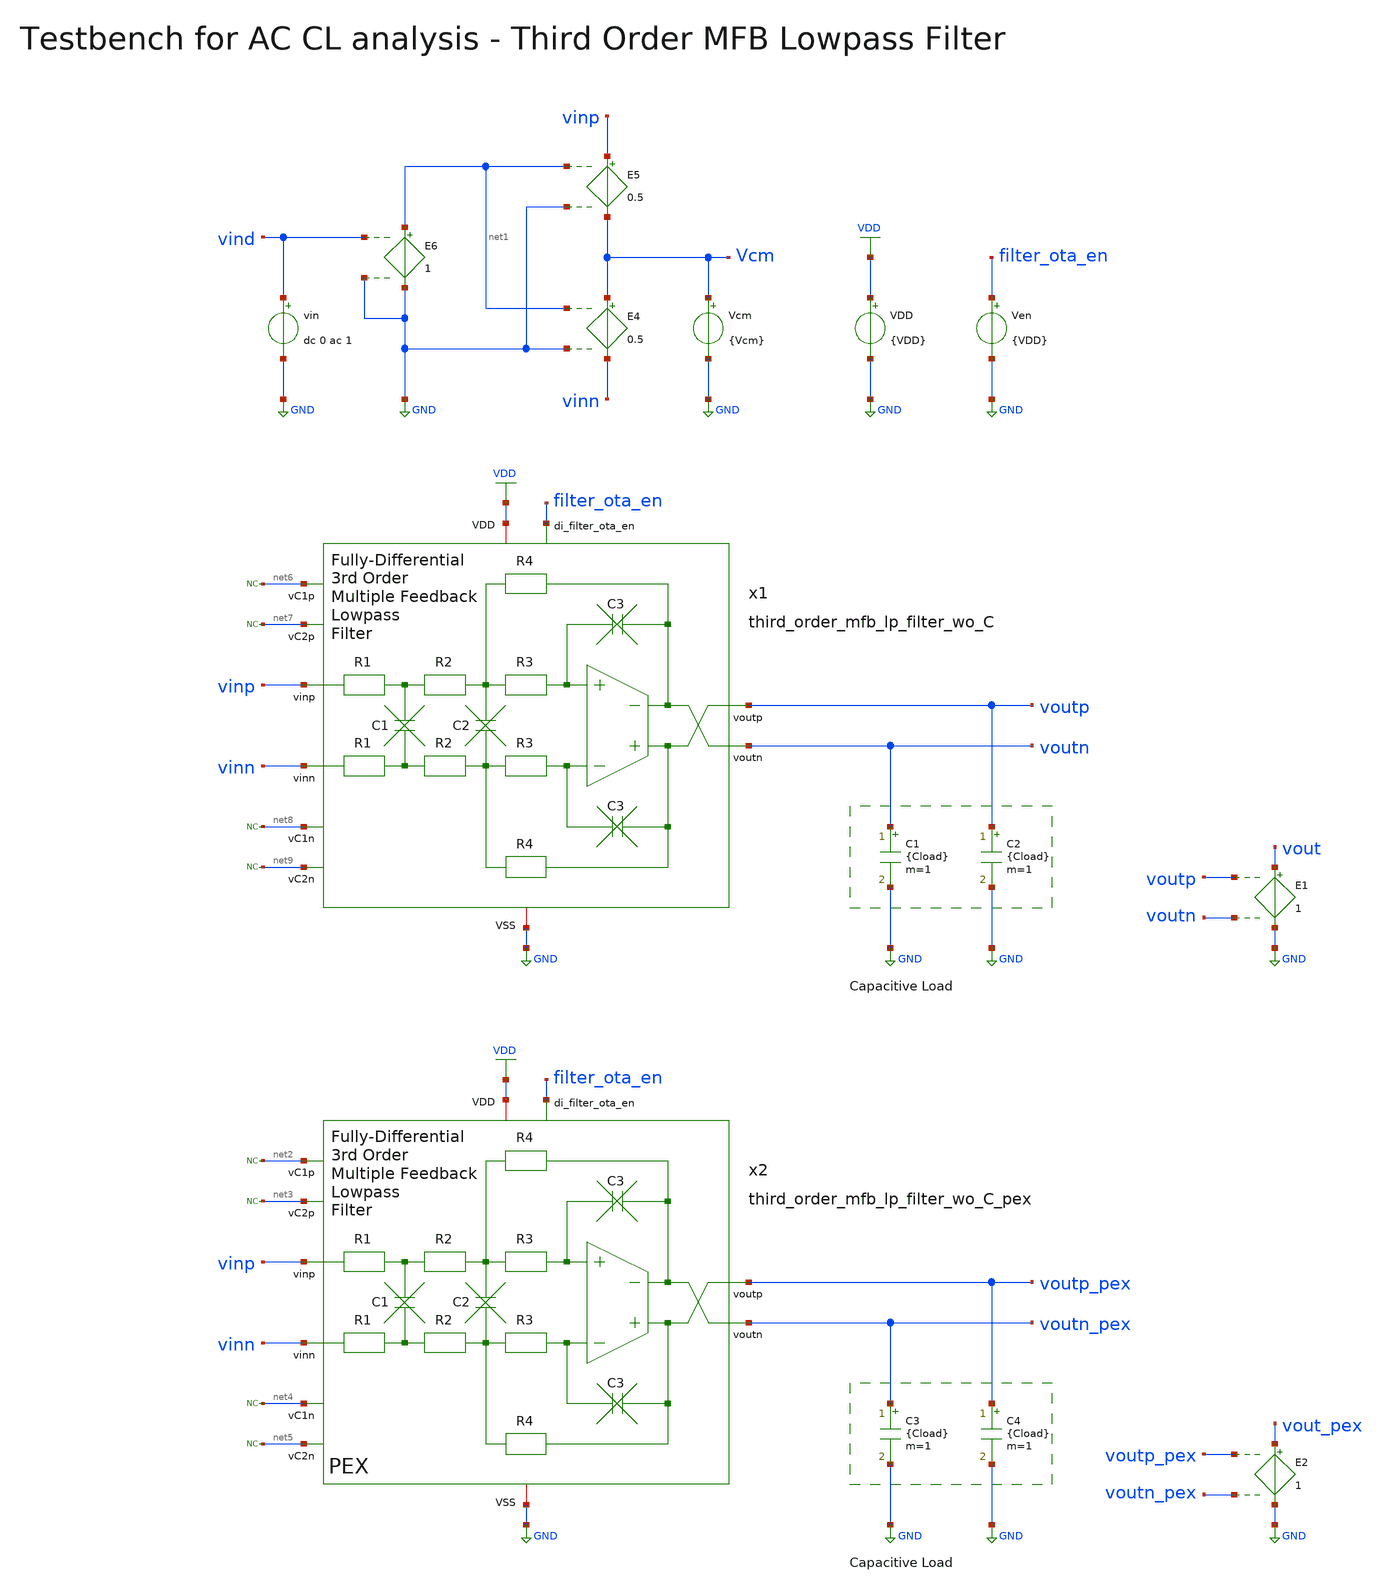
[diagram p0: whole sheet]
** sch_path: magic/iq_modulator/third_order_mfb_lp_filter/third_order_mfb_lp_filter_wo_C_tb_ac_cl.sch
**.subckt third_order_mfb_lp_filter_wo_C_tb_ac_cl
VDD VDD GND {VDD}
C1 voutn GND {Cload} m=1
C2 voutp GND {Cload} m=1
Vcm Vcm GND {Vcm}
E4 Vcm vinn net1 GND 0.5
E5 vinp Vcm net1 GND 0.5
E6 net1 GND vind GND 1
Ven filter_ota_en GND {VDD}
E1 vout GND voutp voutn 1
vin vind GND dc 0 ac 1
x1 filter_ota_en voutp vinp voutn vinn VDD GND net7 net6 net9 net8 third_order_mfb_lp_filter_wo_C
C3 voutn_pex GND {Cload} m=1
C4 voutp_pex GND {Cload} m=1
E2 vout_pex GND voutp_pex voutn_pex 1
* noconn #net6
* noconn #net7
* noconn #net8
* noconn #net9
* noconn #net2
* noconn #net3
* noconn #net4
* noconn #net5
x2 vinp vinn net2 net4 net5 net3 filter_ota_en voutn_pex voutp_pex VDD GND
+ third_order_mfb_lp_filter_wo_C_pex
**** begin user architecture code


.include /foss/designs/TinyWhisper/magic/third_order_mfb_lp_filter/third_order_mfb_lp_filter_wo_C_pex.spice
.param VDD=1.8
.param Vcm=VDD/2
.param temp=27
.param Cload=1p
.options savecurrents klu method=gear reltol=1e-3 abstol=1e-15 gmin=1e-15
.control

save all

set wr_vecnames
set wr_singlescale

* User Constants
let f_min = 1
let f_max = 1G
let fdc = 10

* Operating Point Analysis
* optran 0 0 0 1u 1m 0
op
remzerovec
write third_order_mfb_lp_filter_wo_C_tb_ac_cl.raw
set appendwrite

* AC Analysis
ac dec 101 $&const.f_min $&const.f_max
remzerovec
write third_order_mfb_lp_filter_wo_C_tb_ac_cl.raw
set appendwrite

* Plotting (ideal, PEX)
let Amag = v(vout)/v(vind)
let Amag_dB = vdb(Amag)
let Aarg = 180/PI*cphase(Amag)

let Amag_PEX = v(vout_pex)/v(vind)
let Amag_dB_PEX = vdb(Amag_PEX)
let Aarg_PEX = 180/PI*cphase(Amag_PEX)

plot Amag_dB Amag_dB_PEX ylabel 'Magnitude'
plot Aarg Aarg_PEX ylabel 'Phase'

*quit
.endc


.lib $::SKYWATER_MODELS/sky130.lib.spice tt
**** end user architecture code
**.ends
.GLOBAL GND
.GLOBAL VDD
.end
